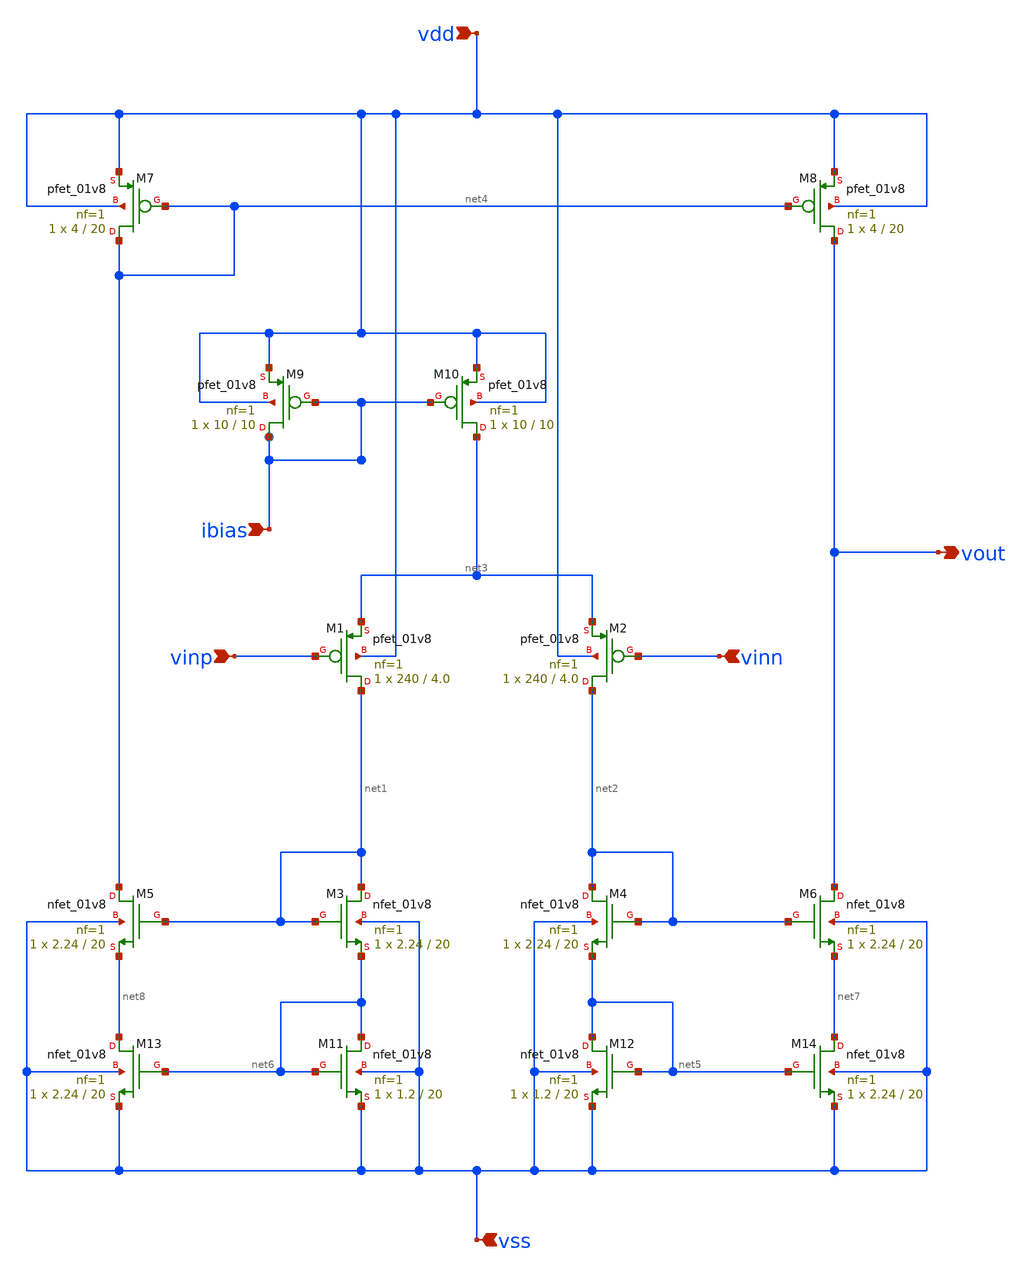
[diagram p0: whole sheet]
** sch_path: Schematic/OTA1.sch
**.subckt OTA1 vdd vinp vinn vss vout ibias
*.ipin vdd
*.ipin vinp
*.ipin vinn
*.ipin vss
*.opin vout
*.ipin ibias
XM1 net1 vinp net3 vdd sky130_fd_pr__pfet_01v8 L=4.0 W=240 nf=1 ad='int((1 + 1)/2) * 240 / 1 * 0.29'
+ as='int((1 + 2)/2) * 240 / 1 * 0.29' pd='2*int((1 + 1)/2) * (240 / 1 + 0.29)' ps='2*int((1 + 2)/2) * (240 / 1 + 0.29)'
+ nrd='0.29 / 240 ' nrs='0.29 / 240 ' sa=0 sb=0 sd=0 mult=1 m=1
XM3 net1 net1 net6 vss sky130_fd_pr__nfet_01v8 L=20 W=2.24 nf=1 ad='int((1 + 1)/2) * 2.24 / 1 * 0.29'
+ as='int((1 + 2)/2) * 2.24 / 1 * 0.29' pd='2*int((1 + 1)/2) * (2.24 / 1 + 0.29)' ps='2*int((1 + 2)/2) * (2.24 / 1 + 0.29)'
+ nrd='0.29 / 2.24 ' nrs='0.29 / 2.24 ' sa=0 sb=0 sd=0 mult=1 m=1
XM4 net2 net2 net5 vss sky130_fd_pr__nfet_01v8 L=20 W=2.24 nf=1 ad='int((1 + 1)/2) * 2.24 / 1 * 0.29'
+ as='int((1 + 2)/2) * 2.24 / 1 * 0.29' pd='2*int((1 + 1)/2) * (2.24 / 1 + 0.29)' ps='2*int((1 + 2)/2) * (2.24 / 1 + 0.29)'
+ nrd='0.29 / 2.24 ' nrs='0.29 / 2.24 ' sa=0 sb=0 sd=0 mult=1 m=1
XM2 net2 vinn net3 vdd sky130_fd_pr__pfet_01v8 L=4.0 W=240 nf=1 ad='int((1 + 1)/2) * 240 / 1 * 0.29'
+ as='int((1 + 2)/2) * 240 / 1 * 0.29' pd='2*int((1 + 1)/2) * (240 / 1 + 0.29)' ps='2*int((1 + 2)/2) * (240 / 1 + 0.29)'
+ nrd='0.29 / 240 ' nrs='0.29 / 240 ' sa=0 sb=0 sd=0 mult=1 m=1
XM5 net4 net1 net8 vss sky130_fd_pr__nfet_01v8 L=20 W=2.24 nf=1 ad='int((1 + 1)/2) * 2.24 / 1 * 0.29'
+ as='int((1 + 2)/2) * 2.24 / 1 * 0.29' pd='2*int((1 + 1)/2) * (2.24 / 1 + 0.29)' ps='2*int((1 + 2)/2) * (2.24 / 1 + 0.29)'
+ nrd='0.29 / 2.24 ' nrs='0.29 / 2.24 ' sa=0 sb=0 sd=0 mult=1 m=1
XM6 vout net2 net7 vss sky130_fd_pr__nfet_01v8 L=20 W=2.24 nf=1 ad='int((1 + 1)/2) * 2.24 / 1 * 0.29'
+ as='int((1 + 2)/2) * 2.24 / 1 * 0.29' pd='2*int((1 + 1)/2) * (2.24 / 1 + 0.29)' ps='2*int((1 + 2)/2) * (2.24 / 1 + 0.29)'
+ nrd='0.29 / 2.24 ' nrs='0.29 / 2.24 ' sa=0 sb=0 sd=0 mult=1 m=1
XM8 vout net4 vdd vdd sky130_fd_pr__pfet_01v8 L=20 W=4 nf=1 ad='int((1 + 1)/2) * 4 / 1 * 0.29' as='int((1 + 2)/2) * 4 / 1 * 0.29'
+ pd='2*int((1 + 1)/2) * (4 / 1 + 0.29)' ps='2*int((1 + 2)/2) * (4 / 1 + 0.29)' nrd='0.29 / 4 ' nrs='0.29 / 4 '
+ sa=0 sb=0 sd=0 mult=1 m=1
XM9 ibias ibias vdd vdd sky130_fd_pr__pfet_01v8 L=10 W=10 nf=1 ad='int((1 + 1)/2) * 10 / 1 * 0.29' as='int((1 + 2)/2) * 10 / 1 * 0.29'
+ pd='2*int((1 + 1)/2) * (10 / 1 + 0.29)' ps='2*int((1 + 2)/2) * (10 / 1 + 0.29)' nrd='0.29 / 10 ' nrs='0.29 / 10 '
+ sa=0 sb=0 sd=0 mult=1 m=1
XM7 net4 net4 vdd vdd sky130_fd_pr__pfet_01v8 L=20 W=4 nf=1 ad='int((1 + 1)/2) * 4 / 1 * 0.29' as='int((1 + 2)/2) * 4 / 1 * 0.29'
+ pd='2*int((1 + 1)/2) * (4 / 1 + 0.29)' ps='2*int((1 + 2)/2) * (4 / 1 + 0.29)' nrd='0.29 / 4 ' nrs='0.29 / 4 '
+ sa=0 sb=0 sd=0 mult=1 m=1
XM10 net3 ibias vdd vdd sky130_fd_pr__pfet_01v8 L=10 W=10 nf=1 ad='int((1 + 1)/2) * 10 / 1 * 0.29' as='int((1 + 2)/2) * 10 / 1 * 0.29'
+ pd='2*int((1 + 1)/2) * (10 / 1 + 0.29)' ps='2*int((1 + 2)/2) * (10 / 1 + 0.29)' nrd='0.29 / 10 ' nrs='0.29 / 10 '
+ sa=0 sb=0 sd=0 mult=1 m=1
XM11 net6 net6 vss vss sky130_fd_pr__nfet_01v8 L=20 W=1.2 nf=1 ad='int((1 + 1)/2) * 1.2 / 1 * 0.29' as='int((1 + 2)/2) * 1.2 / 1 * 0.29'
+ pd='2*int((1 + 1)/2) * (1.2 / 1 + 0.29)' ps='2*int((1 + 2)/2) * (1.2 / 1 + 0.29)' nrd='0.29 / 1.2 ' nrs='0.29 / 1.2 '
+ sa=0 sb=0 sd=0 mult=1 m=1
XM12 net5 net5 vss vss sky130_fd_pr__nfet_01v8 L=20 W=1.2 nf=1 ad='int((1 + 1)/2) * 1.2 / 1 * 0.29' as='int((1 + 2)/2) * 1.2 / 1 * 0.29'
+ pd='2*int((1 + 1)/2) * (1.2 / 1 + 0.29)' ps='2*int((1 + 2)/2) * (1.2 / 1 + 0.29)' nrd='0.29 / 1.2 ' nrs='0.29 / 1.2 '
+ sa=0 sb=0 sd=0 mult=1 m=1
XM13 net8 net6 vss vss sky130_fd_pr__nfet_01v8 L=20 W=2.24 nf=1 ad='int((1 + 1)/2) * 2.24 / 1 * 0.29'
+ as='int((1 + 2)/2) * 2.24 / 1 * 0.29' pd='2*int((1 + 1)/2) * (2.24 / 1 + 0.29)' ps='2*int((1 + 2)/2) * (2.24 / 1 + 0.29)'
+ nrd='0.29 / 2.24 ' nrs='0.29 / 2.24 ' sa=0 sb=0 sd=0 mult=1 m=1
XM14 net7 net5 vss vss sky130_fd_pr__nfet_01v8 L=20 W=2.24 nf=1 ad='int((1 + 1)/2) * 2.24 / 1 * 0.29'
+ as='int((1 + 2)/2) * 2.24 / 1 * 0.29' pd='2*int((1 + 1)/2) * (2.24 / 1 + 0.29)' ps='2*int((1 + 2)/2) * (2.24 / 1 + 0.29)'
+ nrd='0.29 / 2.24 ' nrs='0.29 / 2.24 ' sa=0 sb=0 sd=0 mult=1 m=1
**.ends
.end
